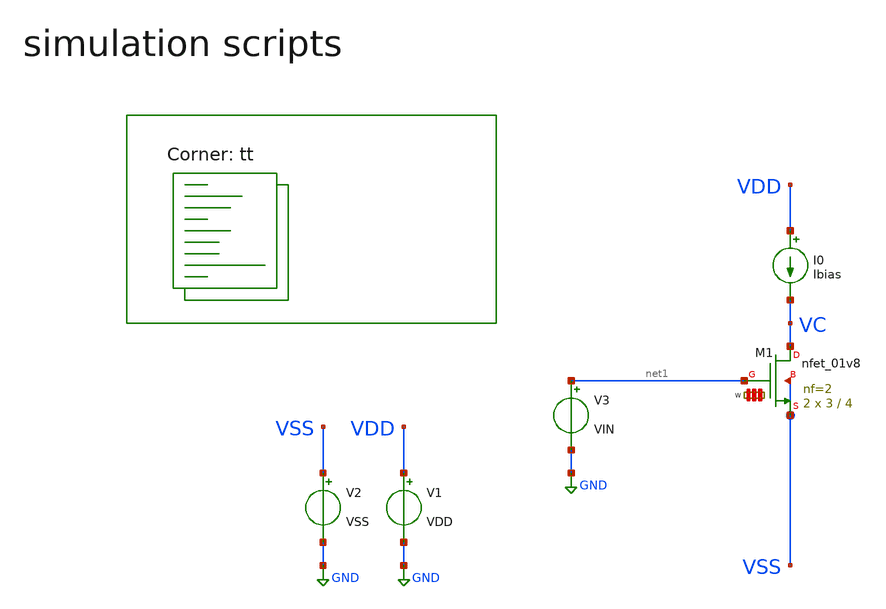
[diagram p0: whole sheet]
** sch_path: my_ip/testbenches_sky/transcondutance_cell/a.sch
**.subckt a
V1 VDD GND VDD
V2 VSS GND VSS
XM1 VC net1 VSS VSS sky130_fd_pr__nfet_01v8 L=4 W='3 * 2 ' nf=2 ad='int((2 + 1)/2) * 3 / 2 * 0.29' as='int((2 + 2)/2) * 3 / 2 * 0.29'
+ pd='2*int((2 + 1)/2) * (3 / 2 + 0.29)' ps='2*int((2 + 2)/2) * (3 / 2 + 0.29)' nrd='0.29 / 3 ' nrs='0.29 / 3 '
+ sa=0 sb=0 sd=0 mult=2 m=2
V3 net1 GND VIN
I0 VDD VC Ibias
**** begin user architecture code
.lib $::SKYWATER_MODELS/sky130.lib.spice tt
**** end user architecture code
**.ends
.GLOBAL GND
**** begin user architecture code



.options savecurrents
.Temp 27
.param VDD = 1.8
.param VSS = 0
.param VIN = 0.9
.param Ibias = 10u


.control
save all
save @m.xm1.msky130_fd_pr__nfet_01v8[vth]

op
print v(VC)
print @m.xm1.msky130_fd_pr__nfet_01v8[gm]

.endc



**** end user architecture code
.end
